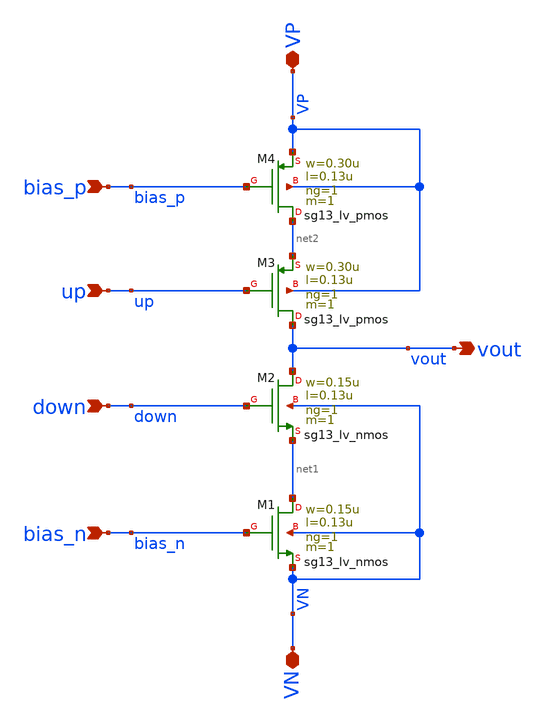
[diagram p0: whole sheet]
** sch_path: Combined Design/design_data/xschem/charge_pump.sch
**.subckt charge_pump bias_p up down bias_n VN VP vout
*.ipin bias_p
*.ipin up
*.ipin down
*.ipin bias_n
*.iopin VN
*.iopin VP
*.opin vout
XM1 net1 bias_n VN VN sg13_lv_nmos w=0.15u l=0.13u ng=1 m=1 mm_ok=1
XM2 vout down net1 VN sg13_lv_nmos w=0.15u l=0.13u ng=1 m=1 mm_ok=1
XM3 vout up net2 VP sg13_lv_pmos w=0.30u l=0.13u ng=1 m=1 mm_ok=1
XM4 net2 bias_p VP VP sg13_lv_pmos w=0.30u l=0.13u ng=1 m=1 mm_ok=1
**.ends
.end
